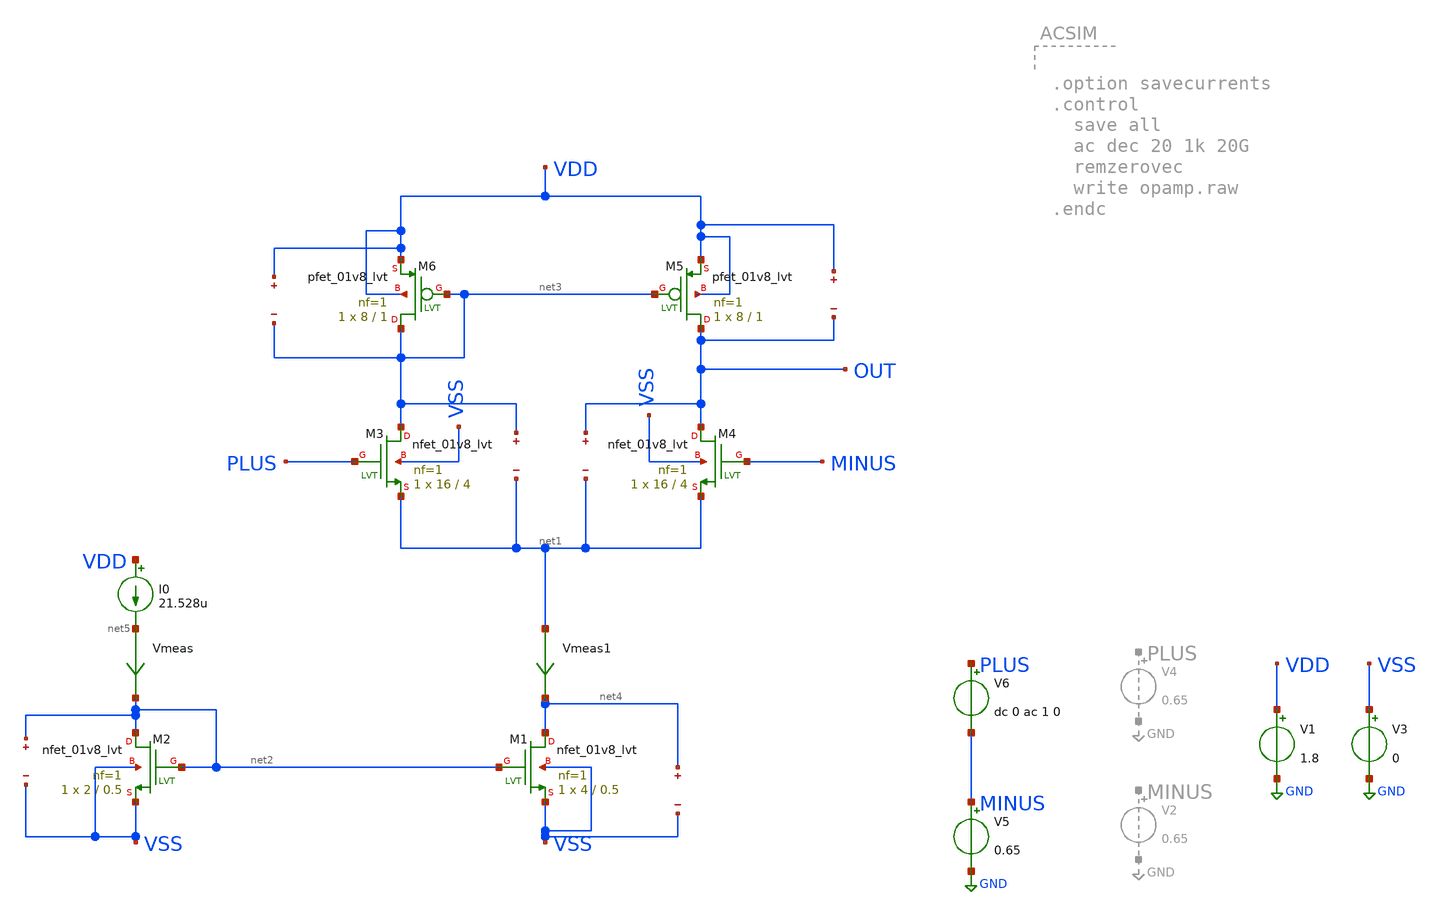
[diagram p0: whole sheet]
** sch_path: custom_gds/tt_um_bgr_agolmanesh/xschem/opamp.sch
**.subckt opamp
XM4 OUT MINUS net1 VSS sky130_fd_pr__nfet_01v8_lvt L=4 W=16 nf=1 ad='int((nf+1)/2) * W/nf * 0.29' as='int((nf+2)/2) * W/nf * 0.29'
+ pd='2*int((nf+1)/2) * (W/nf + 0.29)' ps='2*int((nf+2)/2) * (W/nf + 0.29)' nrd='0.29 / W' nrs='0.29 / W'
+ sa=0 sb=0 sd=0 mult=1 m=1
XM3 net3 PLUS net1 VSS sky130_fd_pr__nfet_01v8_lvt L=4 W=16 nf=1 ad='int((nf+1)/2) * W/nf * 0.29' as='int((nf+2)/2) * W/nf * 0.29'
+ pd='2*int((nf+1)/2) * (W/nf + 0.29)' ps='2*int((nf+2)/2) * (W/nf + 0.29)' nrd='0.29 / W' nrs='0.29 / W'
+ sa=0 sb=0 sd=0 mult=1 m=1
XM5 OUT net3 VDD VDD sky130_fd_pr__pfet_01v8_lvt L=1 W=8 nf=1 ad='int((nf+1)/2) * W/nf * 0.29' as='int((nf+2)/2) * W/nf * 0.29'
+ pd='2*int((nf+1)/2) * (W/nf + 0.29)' ps='2*int((nf+2)/2) * (W/nf + 0.29)' nrd='0.29 / W' nrs='0.29 / W'
+ sa=0 sb=0 sd=0 mult=1 m=1
.save v(out)
.save v(net1)
.save v(net3)
.save v(net1)
V1 VDD GND 1.8
V3 VSS GND 0
I0 VDD net5 21.528u
Vmeas net5 net2 0
.save i(vmeas)
XM1 net4 net2 VSS VSS sky130_fd_pr__nfet_01v8_lvt L=0.5 W=4 nf=1 ad='int((nf+1)/2) * W/nf * 0.29' as='int((nf+2)/2) * W/nf * 0.29'
+ pd='2*int((nf+1)/2) * (W/nf + 0.29)' ps='2*int((nf+2)/2) * (W/nf + 0.29)' nrd='0.29 / W' nrs='0.29 / W'
+ sa=0 sb=0 sd=0 mult=1 m=1
XM2 net2 net2 VSS VSS sky130_fd_pr__nfet_01v8_lvt L=0.5 W=2 nf=1 ad='int((nf+1)/2) * W/nf * 0.29' as='int((nf+2)/2) * W/nf * 0.29'
+ pd='2*int((nf+1)/2) * (W/nf + 0.29)' ps='2*int((nf+2)/2) * (W/nf + 0.29)' nrd='0.29 / W' nrs='0.29 / W'
+ sa=0 sb=0 sd=0 mult=1 m=1
XM6 net3 net3 VDD VDD sky130_fd_pr__pfet_01v8_lvt L=1 W=8 nf=1 ad='int((nf+1)/2) * W/nf * 0.29' as='int((nf+2)/2) * W/nf * 0.29'
+ pd='2*int((nf+1)/2) * (W/nf + 0.29)' ps='2*int((nf+2)/2) * (W/nf + 0.29)' nrd='0.29 / W' nrs='0.29 / W'
+ sa=0 sb=0 sd=0 mult=1 m=1
.save v(vdd)
.save v(net3)
.save v(vdd)
.save v(out)
.save v(net4)
.save v(vss)
.save v(net2)
.save v(vss)
Vmeas1 net1 net4 0
.save i(vmeas1)
V5 MINUS GND 0.65
V6 PLUS MINUS dc 0 ac 1 0
**** begin user architecture code

** opencircuitdesign pdks install
.lib $::SKYWATER_MODELS/sky130.lib.spice tt


**** end user architecture code
**.ends
.GLOBAL GND
**** begin user architecture code


* ngspice commands
.options savecurrents
.control

save @m.xm1.msky130_fd_pr__npet_01v8_lvt[gm]
save @m.xm1.msky130_fd_pr__nfet_01v8_lvt[id]
save @m.xm1.msky130_fd_pr__nfet_01v8_lvt[vgs]
save @m.xm1.msky130_fd_pr__nfet_01v8_lvt[vds]
save @m.xm1.msky130_fd_pr__nfet_01v8_lvt[cgg]
save @m.xm1.msky130_fd_pr__nfet_01v8_lvt[vdsat]
save @m.xm1.msky130_fd_pr__nfet_01v8_lvt[vth]


save @m.xm2.msky130_fd_pr__nfet_01v8_lvt[gm]
save @m.xm2.msky130_fd_pr__nfet_01v8_lvt[id]
save @m.xm2.msky130_fd_pr__nfet_01v8_lvt[vgs]
save @m.xm2.msky130_fd_pr__nfet_01v8_lvt[vds]
save @m.xm2.msky130_fd_pr__nfet_01v8_lvt[cgg]
save @m.xm2.msky130_fd_pr__nfet_01v8_lvt[vdsat]
save @m.xm2.msky130_fd_pr__nfet_01v8_lvt[vth]


save @m.xm3.msky130_fd_pr__nfet_01v8_lvt[gm]
save @m.xm3.msky130_fd_pr__nfet_01v8_lvt[id]
save @m.xm3.msky130_fd_pr__nfet_01v8_lvt[vgs]
save @m.xm3.msky130_fd_pr__nfet_01v8_lvt[vds]
save @m.xm3.msky130_fd_pr__nfet_01v8_lvt[cgg]
save @m.xm3.msky130_fd_pr__nfet_01v8_lvt[vdsat]
save @m.xm3.msky130_fd_pr__nfet_01v8_lvt[vth]


save @m.xm4.msky130_fd_pr__nfet_01v8_lvt[gm]
save @m.xm4.msky130_fd_pr__nfet_01v8_lvt[gds]
save @m.xm4.msky130_fd_pr__nfet_01v8_lvt[id]
save @m.xm4.msky130_fd_pr__nfet_01v8_lvt[vgs]
save @m.xm4.msky130_fd_pr__nfet_01v8_lvt[vds]
save @m.xm4.msky130_fd_pr__nfet_01v8_lvt[cgg]
save @m.xm4.msky130_fd_pr__nfet_01v8_lvt[vdsat]
save @m.xm4.msky130_fd_pr__nfet_01v8_lvt[vth]


save @m.xm5.msky130_fd_pr__pfet_01v8_lvt[gm]
save @m.xm5.msky130_fd_pr__pfet_01v8_lvt[gds]
save @m.xm5.msky130_fd_pr__pfet_01v8_lvt[id]
save @m.xm5.msky130_fd_pr__pfet_01v8_lvt[vgs]
save @m.xm5.msky130_fd_pr__pfet_01v8_lvt[vds]
save @m.xm5.msky130_fd_pr__pfet_01v8_lvt[cgg]
save @m.xm5.msky130_fd_pr__pfet_01v8_lvt[vdsat]
save @m.xm5.msky130_fd_pr__pfet_01v8_lvt[vth]


save @m.xm6.msky130_fd_pr__pfet_01v8_lvt[gm]
save @m.xm6.msky130_fd_pr__pfet_01v8_lvt[id]
save @m.xm6.msky130_fd_pr__pfet_01v8_lvt[vgs]
save @m.xm6.msky130_fd_pr__pfet_01v8_lvt[vds]
save @m.xm6.msky130_fd_pr__pfet_01v8_lvt[cgg]
save @m.xm6.msky130_fd_pr__pfet_01v8_lvt[vdsat]
save @m.xm6.msky130_fd_pr__pfet_01v8_lvt[vth]



save all
op
write opamp.raw
.endc



**** end user architecture code
.end
